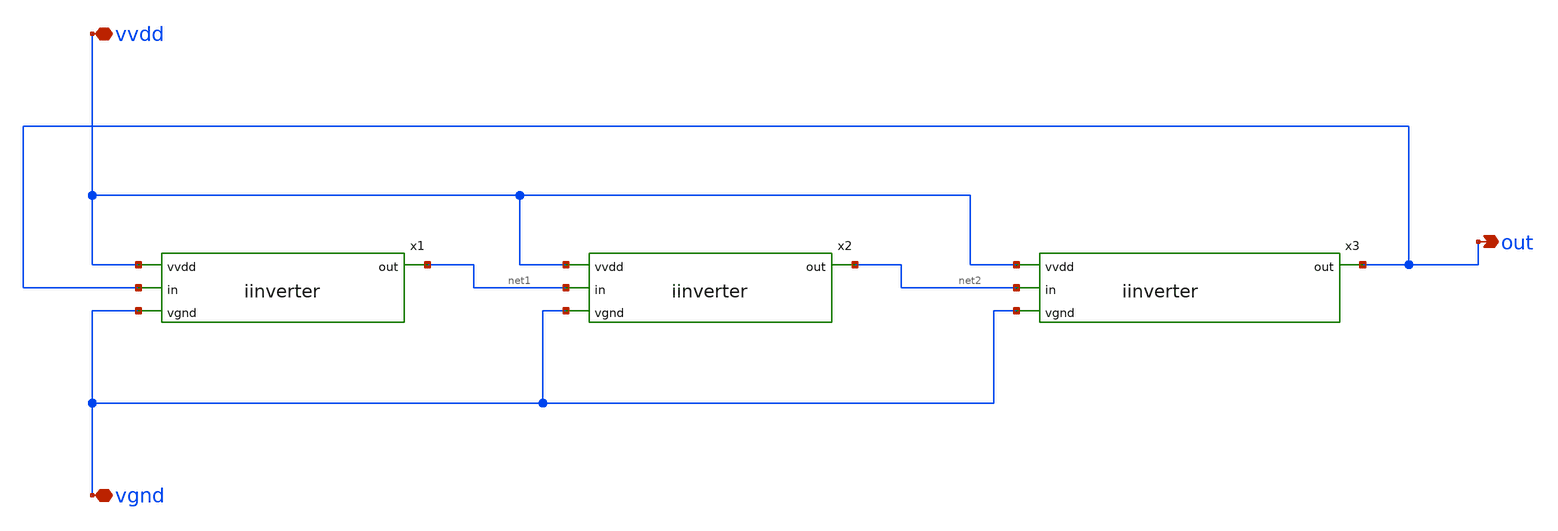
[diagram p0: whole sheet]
** sch_path: oscillator/ring_oscillator.sch
**.subckt ring_oscillator vvdd vgnd out
*.iopin vvdd
*.iopin vgnd
*.opin out
x1 vvdd out net1 vgnd iinverter
x2 vvdd net1 net2 vgnd iinverter
x3 vvdd net2 out vgnd iinverter
**.ends

* expanding   symbol:  /home/deboradmk/project1/iinverter.sym # of pins=4
** sym_path: iinverter/iinverter.sym
** sch_path: iinverter/iinverter.sch
.subckt iinverter vvdd in out vgnd
*.ipin vvdd
*.ipin in
*.ipin vgnd
*.opin out
XM3 out in vgnd vgnd sky130_fd_pr__nfet_01v8 L=0.15 W=1 nf=1 ad='int((nf+1)/2) * W/nf * 0.29' as='int((nf+2)/2) * W/nf * 0.29'
+ pd='2*int((nf+1)/2) * (W/nf + 0.29)' ps='2*int((nf+2)/2) * (W/nf + 0.29)' nrd='0.29 / W' nrs='0.29 / W'
+ sa=0 sb=0 sd=0 mult=1 m=1
XM2 out in vvdd vvdd sky130_fd_pr__pfet_01v8 L=0.15 W=1 nf=1 ad='int((nf+1)/2) * W/nf * 0.29' as='int((nf+2)/2) * W/nf * 0.29'
+ pd='2*int((nf+1)/2) * (W/nf + 0.29)' ps='2*int((nf+2)/2) * (W/nf + 0.29)' nrd='0.29 / W' nrs='0.29 / W'
+ sa=0 sb=0 sd=0 mult=1 m=1
.ends

.end
